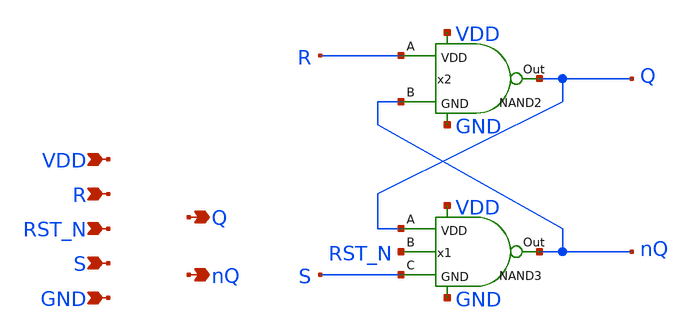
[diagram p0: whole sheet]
** sch_path: src/SR_NAND2.sch
**.subckt SR_NAND2 Q R S VDD GND nQ RST_N
*.opin Q
*.ipin R
*.ipin S
*.ipin VDD
*.ipin GND
*.opin nQ
*.ipin RST_N
x2 R Q nQ VDD GND NAND2
x1 Q nQ S VDD GND RST_N NAND3
**** begin user architecture code

** opencircuitdesign pdks install
.lib $::SKYWATER_MODELS/sky130.lib.spice tt


**** end user architecture code
**.ends

* expanding   symbol:  /foss/designs/PLL2_4/src/NAND2.sym # of pins=5
** sym_path: src/NAND2.sym
** sch_path: src/NAND2.sch
.subckt NAND2 A Out B VDD GND
*.opin Out
*.ipin A
*.ipin B
*.ipin VDD
*.ipin GND
XM1 Out A VDD VDD sky130_fd_pr__pfet_01v8 L=1 W=1 nf=1 ad='int((1 + 1)/2) * 1 / 1 * 0.29' as='int((1 + 2)/2) * 1 / 1 * 0.29'
+ pd='2*int((1 + 1)/2) * (1 / 1 + 0.29)' ps='2*int((1 + 2)/2) * (1 / 1 + 0.29)' nrd='0.29 / 1 ' nrs='0.29 / 1 '
+ sa=0 sb=0 sd=0 mult=1 m=1
XM3 Out B VDD VDD sky130_fd_pr__pfet_01v8 L=1 W=1 nf=1 ad='int((1 + 1)/2) * 1 / 1 * 0.29' as='int((1 + 2)/2) * 1 / 1 * 0.29'
+ pd='2*int((1 + 1)/2) * (1 / 1 + 0.29)' ps='2*int((1 + 2)/2) * (1 / 1 + 0.29)' nrd='0.29 / 1 ' nrs='0.29 / 1 '
+ sa=0 sb=0 sd=0 mult=1 m=1
XM4 net1 B GND GND sky130_fd_pr__nfet_01v8 L=1 W=1 nf=1 ad='int((1 + 1)/2) * 1 / 1 * 0.29' as='int((1 + 2)/2) * 1 / 1 * 0.29'
+ pd='2*int((1 + 1)/2) * (1 / 1 + 0.29)' ps='2*int((1 + 2)/2) * (1 / 1 + 0.29)' nrd='0.29 / 1 ' nrs='0.29 / 1 '
+ sa=0 sb=0 sd=0 mult=1 m=1
XM5 Out A net1 GND sky130_fd_pr__nfet_01v8 L=1 W=1 nf=1 ad='int((1 + 1)/2) * 1 / 1 * 0.29' as='int((1 + 2)/2) * 1 / 1 * 0.29'
+ pd='2*int((1 + 1)/2) * (1 / 1 + 0.29)' ps='2*int((1 + 2)/2) * (1 / 1 + 0.29)' nrd='0.29 / 1 ' nrs='0.29 / 1 '
+ sa=0 sb=0 sd=0 mult=1 m=1
.ends


* expanding   symbol:  /foss/designs/PLL2_4/src/NAND3.sym # of pins=6
** sym_path: src/NAND3.sym
** sch_path: src/NAND3.sch
.subckt NAND3 A Out C VDD GND B
*.opin Out
*.ipin A
*.ipin B
*.ipin VDD
*.ipin GND
*.ipin C
XM1 Out A VDD VDD sky130_fd_pr__pfet_01v8 L=1 W=1 nf=1 ad='int((1 + 1)/2) * 1 / 1 * 0.29' as='int((1 + 2)/2) * 1 / 1 * 0.29'
+ pd='2*int((1 + 1)/2) * (1 / 1 + 0.29)' ps='2*int((1 + 2)/2) * (1 / 1 + 0.29)' nrd='0.29 / 1 ' nrs='0.29 / 1 '
+ sa=0 sb=0 sd=0 mult=1 m=1
XM3 Out C VDD VDD sky130_fd_pr__pfet_01v8 L=1 W=1 nf=1 ad='int((1 + 1)/2) * 1 / 1 * 0.29' as='int((1 + 2)/2) * 1 / 1 * 0.29'
+ pd='2*int((1 + 1)/2) * (1 / 1 + 0.29)' ps='2*int((1 + 2)/2) * (1 / 1 + 0.29)' nrd='0.29 / 1 ' nrs='0.29 / 1 '
+ sa=0 sb=0 sd=0 mult=1 m=1
XM4 net2 C GND GND sky130_fd_pr__nfet_01v8 L=1 W=1 nf=1 ad='int((1 + 1)/2) * 1 / 1 * 0.29' as='int((1 + 2)/2) * 1 / 1 * 0.29'
+ pd='2*int((1 + 1)/2) * (1 / 1 + 0.29)' ps='2*int((1 + 2)/2) * (1 / 1 + 0.29)' nrd='0.29 / 1 ' nrs='0.29 / 1 '
+ sa=0 sb=0 sd=0 mult=1 m=1
XM5 Out A net1 GND sky130_fd_pr__nfet_01v8 L=1 W=1 nf=1 ad='int((1 + 1)/2) * 1 / 1 * 0.29' as='int((1 + 2)/2) * 1 / 1 * 0.29'
+ pd='2*int((1 + 1)/2) * (1 / 1 + 0.29)' ps='2*int((1 + 2)/2) * (1 / 1 + 0.29)' nrd='0.29 / 1 ' nrs='0.29 / 1 '
+ sa=0 sb=0 sd=0 mult=1 m=1
XM2 Out B VDD VDD sky130_fd_pr__pfet_01v8 L=1 W=1 nf=1 ad='int((1 + 1)/2) * 1 / 1 * 0.29' as='int((1 + 2)/2) * 1 / 1 * 0.29'
+ pd='2*int((1 + 1)/2) * (1 / 1 + 0.29)' ps='2*int((1 + 2)/2) * (1 / 1 + 0.29)' nrd='0.29 / 1 ' nrs='0.29 / 1 '
+ sa=0 sb=0 sd=0 mult=1 m=1
XM6 net1 B net2 GND sky130_fd_pr__nfet_01v8 L=1 W=1 nf=1 ad='int((1 + 1)/2) * 1 / 1 * 0.29' as='int((1 + 2)/2) * 1 / 1 * 0.29'
+ pd='2*int((1 + 1)/2) * (1 / 1 + 0.29)' ps='2*int((1 + 2)/2) * (1 / 1 + 0.29)' nrd='0.29 / 1 ' nrs='0.29 / 1 '
+ sa=0 sb=0 sd=0 mult=1 m=1
.ends

.end
